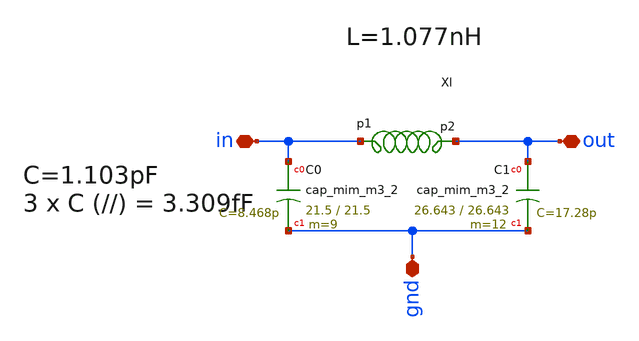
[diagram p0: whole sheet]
** sch_path: impedance-transformer/xschem/impedance-transformer.sch
**.subckt impedance-transformer gnd in out
*.iopin gnd
*.iopin in
*.iopin out
XC0 in gnd sky130_fd_pr__cap_mim_m3_2 W=21.5 L=21.5 MF=9 m=9
XC1 out gnd sky130_fd_pr__cap_mim_m3_2 W=26.643 L=26.643 MF=12 m=12
x1 in out l1
**.ends

* expanding   symbol:  /home/hugodg/projects_sky130/temp_sensor/impedance-transformer/xschem/l1.sym
*+ # of pins=2
** sym_path: impedance-transformer/xschem/l1.sym
** sch_path: impedance-transformer/xschem/l1.sch
.subckt l1 p1 p2
*.iopin p2
*.iopin p1
L0 p1 net3 694.6p m=1
Cs1 p1 net1 15.23f m=1
Cs2 p2 net2 16.88f m=1
Rs1 net1 GND 88.99 m=1
Rs2 net2 GND -52.45 m=1
R1 p2 net3 2.899 m=1
.ends

.GLOBAL GND
.end
